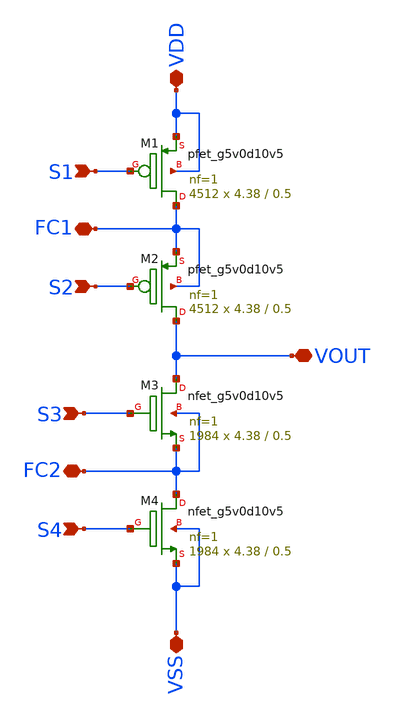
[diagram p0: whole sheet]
** sch_path: xschem/power_stage_1.sch
**.subckt power_stage_1 VDD S1 S2 VOUT S3 S4 VSS FC1 FC2
*.iopin VDD
*.ipin S1
*.ipin S2
*.iopin VOUT
*.ipin S3
*.ipin S4
*.iopin VSS
*.iopin FC1
*.iopin FC2
XM2 VOUT S2 FC1 FC1 sky130_fd_pr__pfet_g5v0d10v5 L=0.5 W=4.38 nf=1 ad='int((nf+1)/2) * W/nf * 0.29' as='int((nf+2)/2) * W/nf * 0.29'
+ pd='2*int((nf+1)/2) * (W/nf + 0.29)' ps='2*int((nf+2)/2) * (W/nf + 0.29)' nrd='0.29 / W' nrs='0.29 / W'
+ sa=0 sb=0 sd=0 mult=4512 m=4512
XM1 FC1 S1 VDD VDD sky130_fd_pr__pfet_g5v0d10v5 L=0.5 W=4.38 nf=1 ad='int((nf+1)/2) * W/nf * 0.29' as='int((nf+2)/2) * W/nf * 0.29'
+ pd='2*int((nf+1)/2) * (W/nf + 0.29)' ps='2*int((nf+2)/2) * (W/nf + 0.29)' nrd='0.29 / W' nrs='0.29 / W'
+ sa=0 sb=0 sd=0 mult=4512 m=4512
XM3 VOUT S3 FC2 FC2 sky130_fd_pr__nfet_g5v0d10v5 L=0.5 W=4.38 nf=1 ad='int((nf+1)/2) * W/nf * 0.29' as='int((nf+2)/2) * W/nf * 0.29'
+ pd='2*int((nf+1)/2) * (W/nf + 0.29)' ps='2*int((nf+2)/2) * (W/nf + 0.29)' nrd='0.29 / W' nrs='0.29 / W'
+ sa=0 sb=0 sd=0 mult=1984 m=1984
XM4 FC2 S4 VSS VSS sky130_fd_pr__nfet_g5v0d10v5 L=0.5 W=4.38 nf=1 ad='int((nf+1)/2) * W/nf * 0.29' as='int((nf+2)/2) * W/nf * 0.29'
+ pd='2*int((nf+1)/2) * (W/nf + 0.29)' ps='2*int((nf+2)/2) * (W/nf + 0.29)' nrd='0.29 / W' nrs='0.29 / W'
+ sa=0 sb=0 sd=0 mult=1984 m=1984
**.ends
.end
